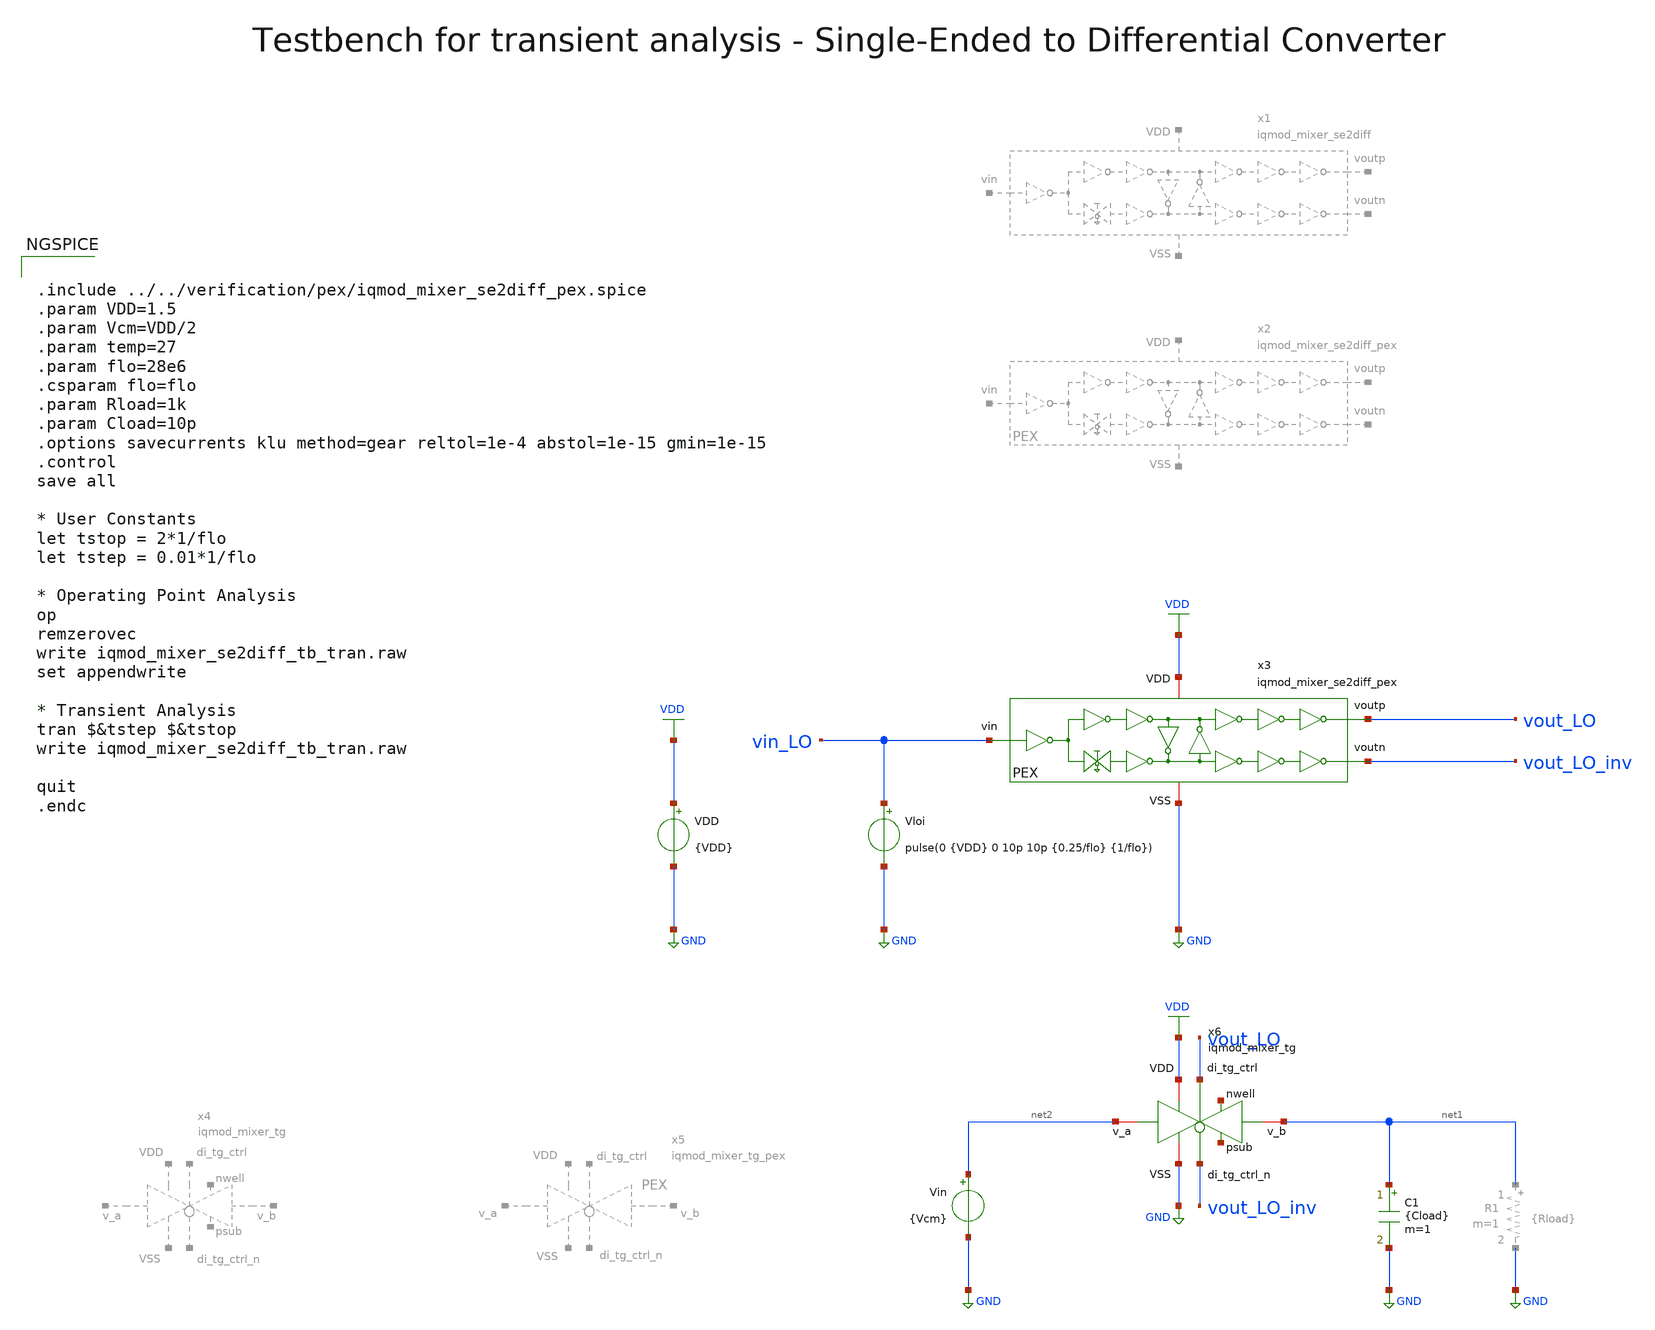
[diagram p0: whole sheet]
** sch_path: ihp130/macros/iqmod/xschem/testbenches/iqmod_mixer_se2diff_tb_tran.sch
**.subckt iqmod_mixer_se2diff_tb_tran
VDD VDD GND {VDD}
C1 net1 GND {Cload} m=1
Vloi vin_LO GND pulse(0 {VDD} 0 10p 10p {0.25/flo} {1/flo})
Vin net2 GND {Vcm}
x6 net3 net4 VDD vout_LO GND net1 net2 vout_LO_inv iqmod_mixer_tg
x3 VDD vin_LO vout_LO GND vout_LO_inv iqmod_mixer_se2diff_pex
**** begin user architecture code


.include ../../verification/pex/iqmod_mixer_se2diff_pex.spice
.param VDD=1.5
.param Vcm=VDD/2
.param temp=27
.param flo=28e6
.csparam flo=flo
.param Rload=1k
.param Cload=10p
.options savecurrents klu method=gear reltol=1e-4 abstol=1e-15 gmin=1e-15
.control
save all

* User Constants
let tstop = 2*1/flo
let tstep = 0.01*1/flo

* Operating Point Analysis
op
remzerovec
write iqmod_mixer_se2diff_tb_tran.raw
set appendwrite

* Transient Analysis
tran $&tstep $&tstop
write iqmod_mixer_se2diff_tb_tran.raw

quit
.endc



.lib cornerMOSlv.lib mos_tt
.lib cornerMOShv.lib mos_tt
.lib cornerHBT.lib hbt_typ
.lib cornerRES.lib res_typ
.lib cornerCAP.lib cap_typ
.lib cornerDIO.lib dio_tt

**** end user architecture code
**.ends
.GLOBAL GND
.GLOBAL VDD
.end
